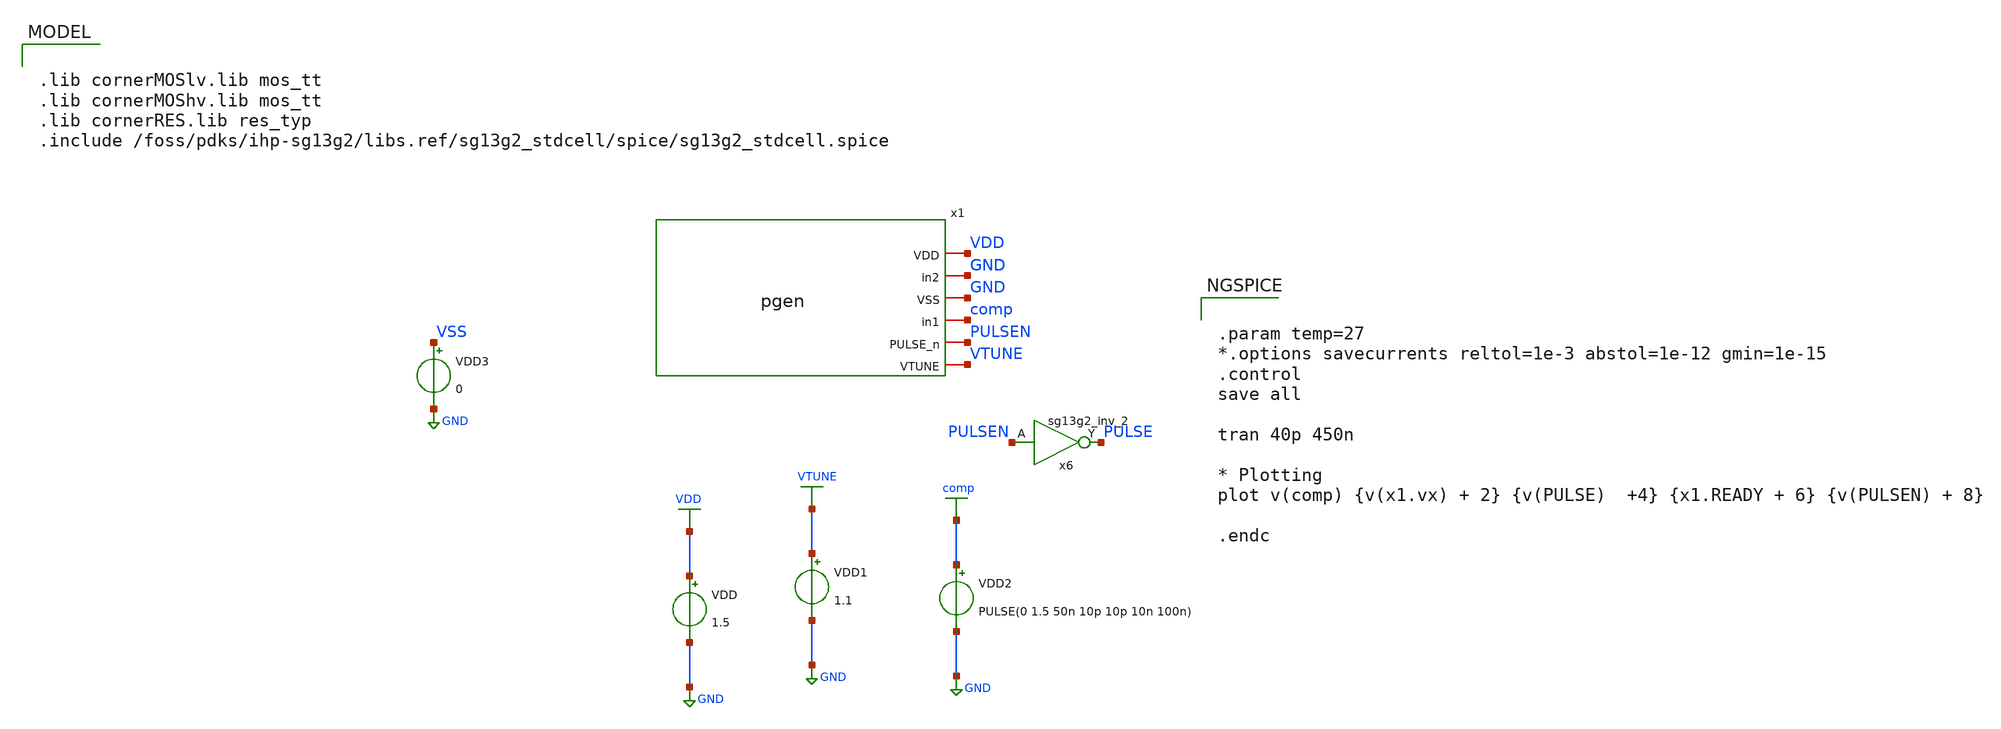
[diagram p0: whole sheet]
** sch_path: xschem/comparator/pulse_gen/testbench/tb_pgen.sch
* IHP-GmbH/IHP-Open-PDK/ihp-sg13g2/libs.tech/xschem/sg13g2_stdcells/sg13g2_inv_2.sch:
* Copyright 2023 IHP PDK Authors
* Licensed under the Apache License, Version 2.0 (the "License");
**.subckt tb_pgen
x1 VDD GND GND comp PULSEN VTUNE pgen
VDD VDD GND 1.5
VDD1 VTUNE GND 1.1
VDD2 comp GND PULSE(0 1.5 50n 10p 10p 10n 100n)
x6 PULSE PULSEN VDD VSS sg13g2_inv_2
VDD3 VSS GND 0
**** begin user architecture code

.lib cornerMOSlv.lib mos_tt
.lib cornerMOShv.lib mos_tt
.lib cornerRES.lib res_typ
.include /foss/pdks/ihp-sg13g2/libs.ref/sg13g2_stdcell/spice/sg13g2_stdcell.spice



.param temp=27
*.options savecurrents reltol=1e-3 abstol=1e-12 gmin=1e-15
.control
save all

tran 40p 450n

* Plotting
plot v(comp) {v(x1.vx) + 2} {v(PULSE)  +4} {x1.READY + 6} {v(PULSEN) + 8}

.endc

**** end user architecture code
**.ends

* expanding   symbol:  comparator/pulse_gen/pgen.sym # of pins=6
** sym_path: xschem/comparator/pulse_gen/pgen.sym
** sch_path: xschem/comparator/pulse_gen/pgen.sch
.subckt pgen VDD in2 VSS in1 PULSE_n VTUNE
*.iopin VDD
*.iopin in2
*.iopin in1
*.iopin VSS
*.iopin VTUNE
*.iopin PULSE_n
XM1 READY in1 VSS VSS sg13_lv_nmos w=0.15u l=0.13u ng=1 m=1 mm_ok=1
XM2 READY vx_n VDD VDD sg13_lv_pmos w=2u l=0.13u ng=1 m=1 mm_ok=1
XM4 vx PULSE_n net5 VDD sg13_lv_pmos w=0.15u l=0.13u ng=1 m=1 mm_ok=1
x46 PULSE_n vxs net1 VDD VSS sg13g2_or2_1
x6 vx_n vxs VDD VSS sg13g2_inv_2
XM3 READY in2 VSS VSS sg13_lv_nmos w=0.15u l=0.13u ng=1 m=1 mm_ok=1
XM5 vx net1 VSS VSS sg13_lv_nmos w=0.15u l=0.13u ng=1 m=1 mm_ok=1
XM7 net5 VTUNE VDD VDD sg13_lv_pmos w=0.15u l=0.13u ng=1 m=1 mm_ok=1
XM6 net4 vx VDD VDD sg13_lv_pmos w=0.15u l=0.13u ng=1 m=1 mm_ok=1
XM8 net3 vx net2 VSS sg13_lv_nmos w=0.15u l=0.13u ng=1 m=1 mm_ok=1
XM9 net3 vx net4 VDD sg13_lv_pmos w=0.15u l=0.13u ng=1 m=1 mm_ok=1
XM10 net2 vx VSS VSS sg13_lv_nmos w=0.15u l=0.13u ng=1 m=1 mm_ok=1
XM11 VDD net3 net2 VDD sg13_lv_nmos w=0.15u l=0.13u ng=1 m=1 mm_ok=1
XM12 VSS net3 net4 VSS sg13_lv_pmos w=0.15u l=0.13u ng=1 m=1 mm_ok=1
x1 vxs net3 VDD VSS sg13g2_inv_2
x2 net6 READY VDD VSS sg13g2_inv_2
x3 net1 net6 VDD VSS sg13g2_inv_2
.ends


* expanding   symbol:  sg13g2_stdcells/sg13g2_inv_2.sym # of pins=2
** sym_path: sg13g2_stdcells/sg13g2_inv_2.sym
** sch_path: sg13g2_stdcells/sg13g2_inv_2.sch
.subckt sg13g2_inv_2 Y A VDD VSS
*.opin Y
*.ipin A
*.iopin VDD
*.iopin VSS
XM1 Y A VSS VSS sg13_lv_nmos w=1.48u l=130.00n ng=2 m=1 mm_ok=1
XM2 Y A VDD VDD sg13_lv_pmos w=2.24u l=130.00n ng=2 m=1 mm_ok=1
.ends


* expanding   symbol:  sg13g2_stdcells/sg13g2_or2_1.sym # of pins=3
** sym_path: sg13g2_stdcells/sg13g2_or2_1.sym
** sch_path: sg13g2_stdcells/sg13g2_or2_1.sch
.subckt sg13g2_or2_1 X A B VDD VSS
*.opin X
*.ipin B
*.ipin A
*.iopin VDD
*.iopin VSS
XM1 net1 B VSS VSS sg13_lv_nmos w=550.00n l=130.00n ng=1 m=1 mm_ok=1
XM2 net1 A VSS VSS sg13_lv_nmos w=550.00n l=130.00n ng=1 m=1 mm_ok=1
XM3 X net1 VSS VSS sg13_lv_nmos w=740.00n l=130.00n ng=1 m=1 mm_ok=1
XM4 net2 A VDD VDD sg13_lv_pmos w=840.00n l=130.00n ng=1 m=1 mm_ok=1
XM5 net1 B net2 VDD sg13_lv_pmos w=840.00n l=130.00n ng=1 m=1 mm_ok=1
XM6 X net1 VDD VDD sg13_lv_pmos w=1.12u l=130.00n ng=1 m=1 mm_ok=1
.ends

.GLOBAL GND
.GLOBAL VDD
.GLOBAL VTUNE
.GLOBAL comp
.end
